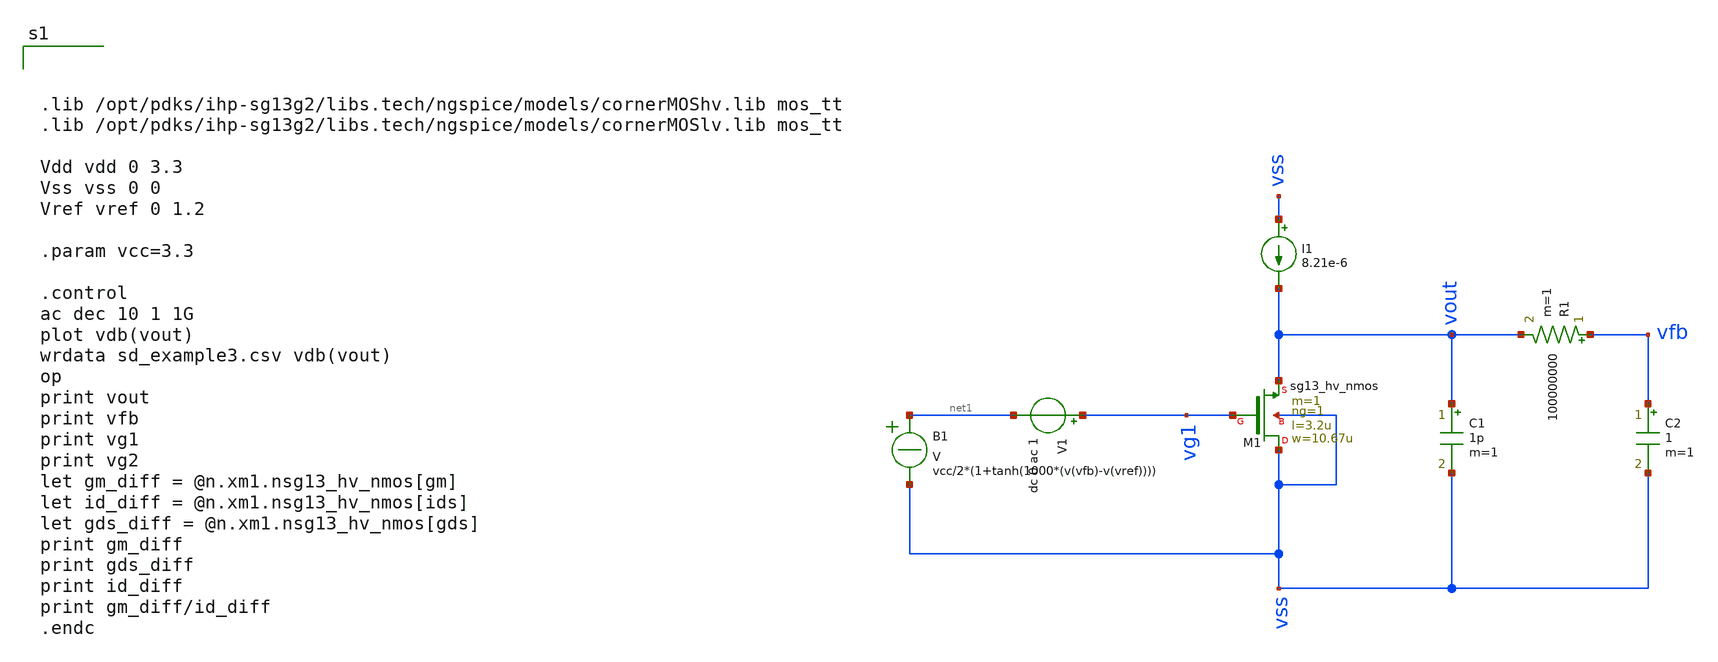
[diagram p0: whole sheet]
** sch_path: test-python/sstadex/xschem/sd_example3.sch
**.subckt sd_example3
XM1 vss vg1 vout vss sg13_hv_nmos w=10.67u l=3.2u ng=1 m=1 mm_ok=1
C1 vout vss 1p m=1
I1 vss vout 8.21e-6
B1 net1 vss V = vcc/2*(1+tanh(1000*(v(vfb)-v(vref))))
V1 vg1 net1 dc 0 ac 1
R1 vfb vout 100000000 m=1
C2 vfb vss 1 m=1
**** begin user architecture code



.lib /opt/pdks/ihp-sg13g2/libs.tech/ngspice/models/cornerMOShv.lib mos_tt
.lib /opt/pdks/ihp-sg13g2/libs.tech/ngspice/models/cornerMOSlv.lib mos_tt

Vdd vdd 0 3.3
Vss vss 0 0
Vref vref 0 1.2

.param vcc=3.3

.control
ac dec 10 1 1G
plot vdb(vout)
wrdata sd_example3.csv vdb(vout)
op
print vout
print vfb
print vg1
print vg2
let gm_diff = @n.xm1.nsg13_hv_nmos[gm]
let id_diff = @n.xm1.nsg13_hv_nmos[ids]
let gds_diff = @n.xm1.nsg13_hv_nmos[gds]
print gm_diff
print gds_diff
print id_diff
print gm_diff/id_diff
.endc



**** end user architecture code
**.ends
.end
